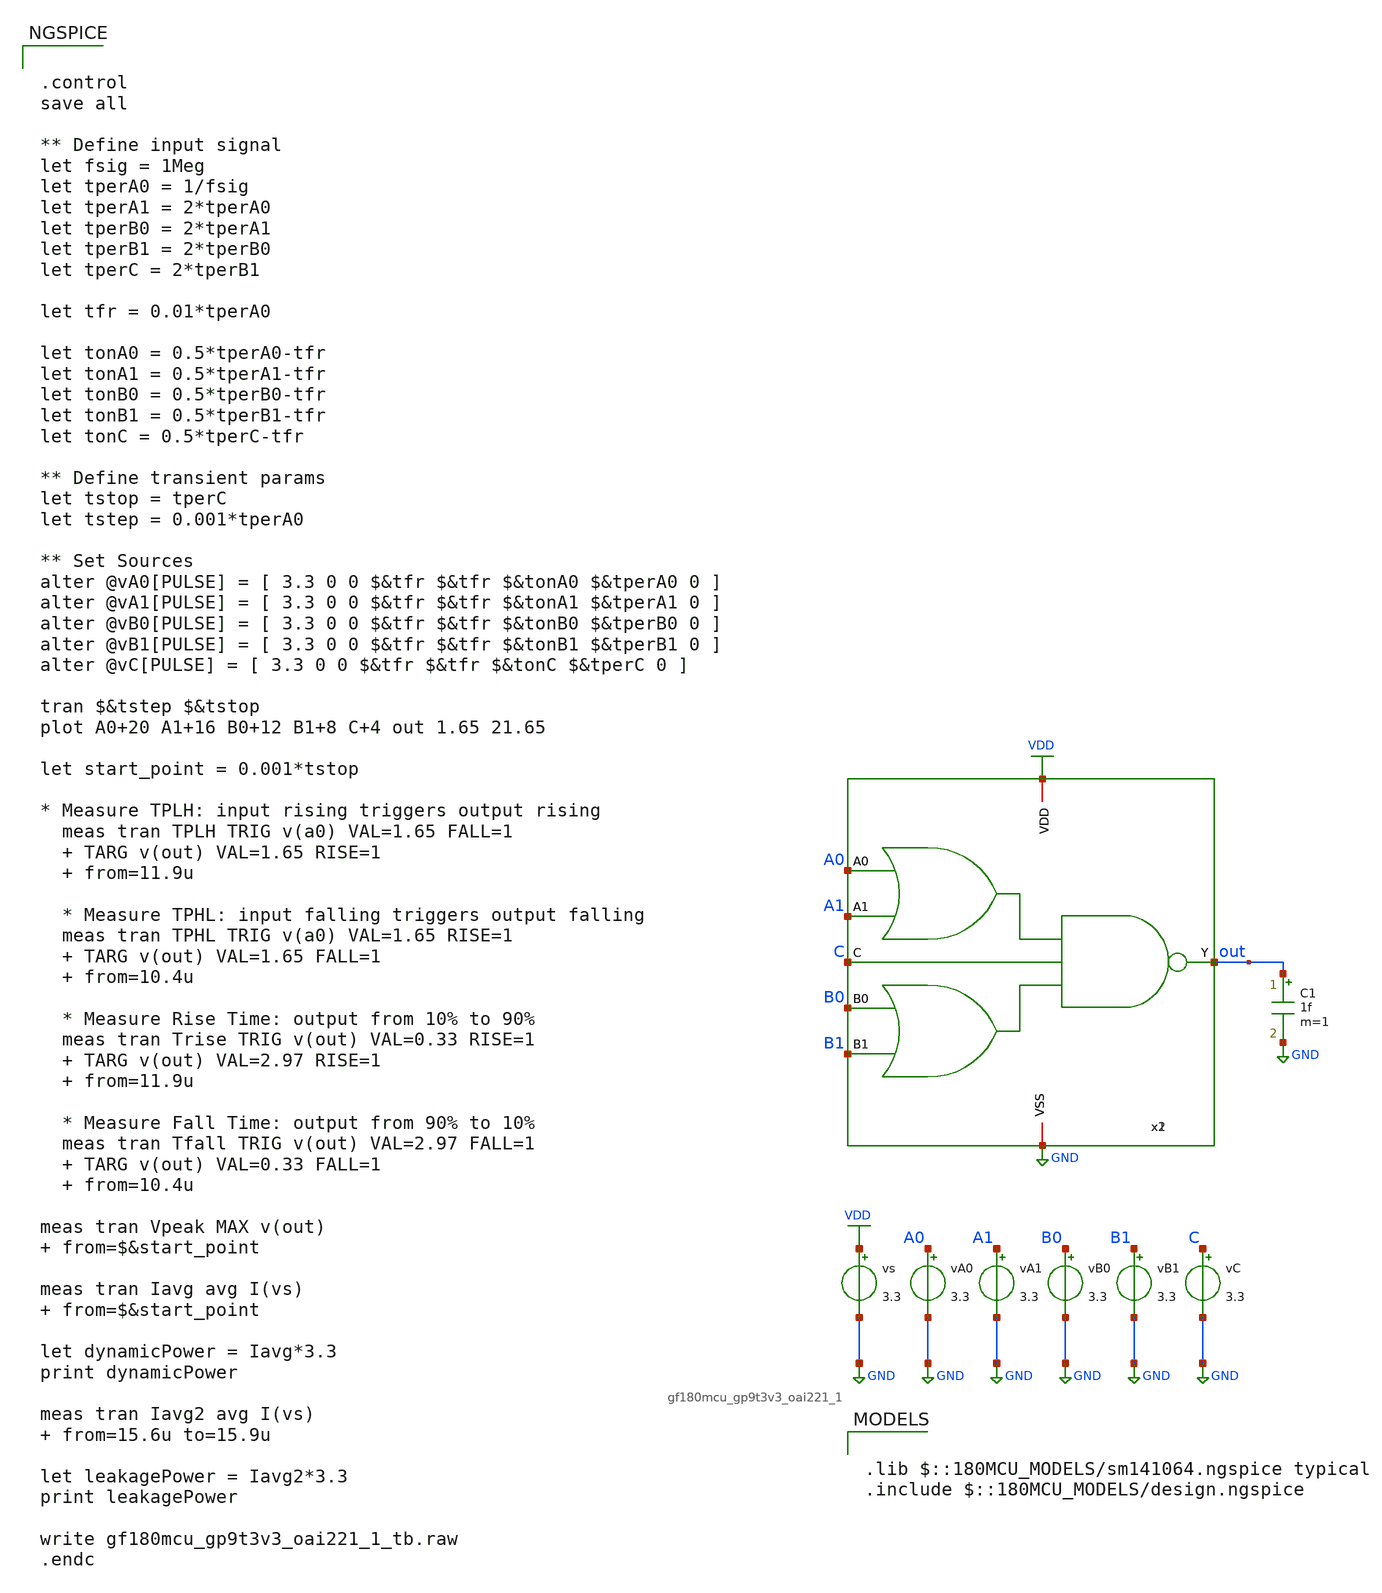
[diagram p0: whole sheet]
** sch_path: designs/oai221/gf180mcu_gp9t3v3_oai221_1_tb.sch
**.subckt gf180mcu_gp9t3v3_oai221_1_tb
vA0 A0 GND 3.3
vs VDD GND 3.3
vA1 A1 GND 3.3
vB1 B1 GND 3.3
vB0 B0 GND 3.3
vC C GND 3.3
C1 out GND 1f m=1
x1 VDD A0 B0 C A1 B1 out GND gf180mcu_gp9t3v3_oai221_1
x2 VDD A0 B0 C A1 B1 out GND gf180mcu_gp9t3v3_oai221_1
**** begin user architecture code


.control
save all

** Define input signal
let fsig = 1Meg
let tperA0 = 1/fsig
let tperA1 = 2*tperA0
let tperB0 = 2*tperA1
let tperB1 = 2*tperB0
let tperC = 2*tperB1

let tfr = 0.01*tperA0

let tonA0 = 0.5*tperA0-tfr
let tonA1 = 0.5*tperA1-tfr
let tonB0 = 0.5*tperB0-tfr
let tonB1 = 0.5*tperB1-tfr
let tonC = 0.5*tperC-tfr

** Define transient params
let tstop = tperC
let tstep = 0.001*tperA0

** Set Sources
alter @vA0[PULSE] = [ 3.3 0 0 $&tfr $&tfr $&tonA0 $&tperA0 0 ]
alter @vA1[PULSE] = [ 3.3 0 0 $&tfr $&tfr $&tonA1 $&tperA1 0 ]
alter @vB0[PULSE] = [ 3.3 0 0 $&tfr $&tfr $&tonB0 $&tperB0 0 ]
alter @vB1[PULSE] = [ 3.3 0 0 $&tfr $&tfr $&tonB1 $&tperB1 0 ]
alter @vC[PULSE] = [ 3.3 0 0 $&tfr $&tfr $&tonC $&tperC 0 ]

tran $&tstep $&tstop
plot A0+20 A1+16 B0+12 B1+8 C+4 out 1.65 21.65

let start_point = 0.001*tstop

* Measure TPLH: input rising triggers output rising
  meas tran TPLH TRIG v(a0) VAL=1.65 FALL=1
  + TARG v(out) VAL=1.65 RISE=1
  + from=11.9u

  * Measure TPHL: input falling triggers output falling
  meas tran TPHL TRIG v(a0) VAL=1.65 RISE=1
  + TARG v(out) VAL=1.65 FALL=1
  + from=10.4u

  * Measure Rise Time: output from 10% to 90%
  meas tran Trise TRIG v(out) VAL=0.33 RISE=1
  + TARG v(out) VAL=2.97 RISE=1
  + from=11.9u

  * Measure Fall Time: output from 90% to 10%
  meas tran Tfall TRIG v(out) VAL=2.97 FALL=1
  + TARG v(out) VAL=0.33 FALL=1
  + from=10.4u

meas tran Vpeak MAX v(out)  from=$&start_point

meas tran Iavg avg I(vs)  from=$&start_point

let dynamicPower = Iavg*3.3
print dynamicPower

meas tran Iavg2 avg I(vs)  from=15.6u to=15.9u

let leakagePower = Iavg2*3.3
print leakagePower

write gf180mcu_gp9t3v3_oai221_1_tb.raw
.endc



.lib $::180MCU_MODELS/sm141064.ngspice typical
.include $::180MCU_MODELS/design.ngspice

**** end user architecture code
**.ends
.GLOBAL VDD
.GLOBAL GND
.end
